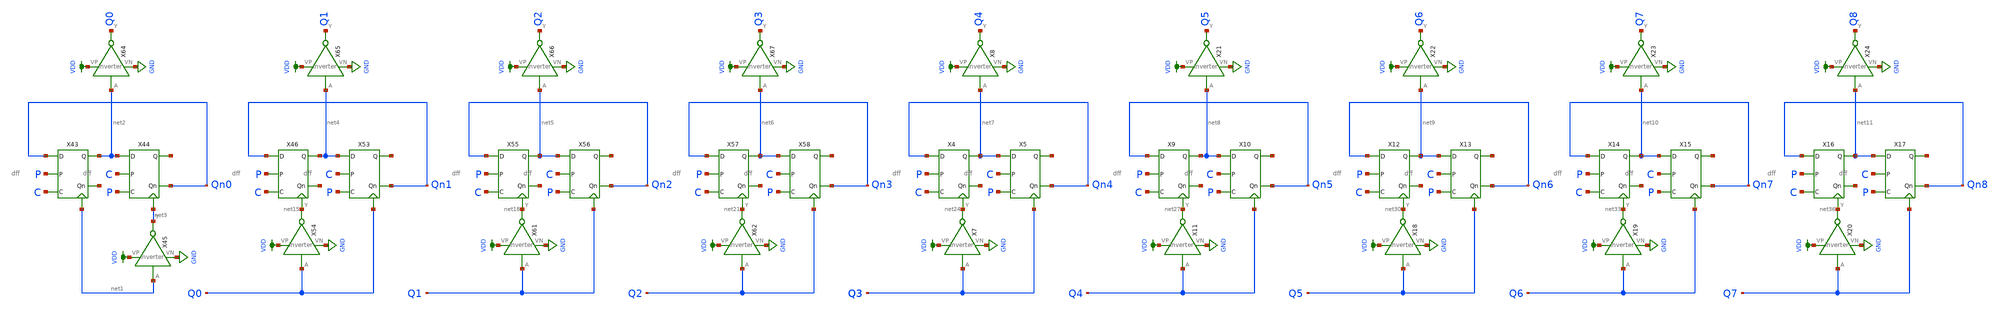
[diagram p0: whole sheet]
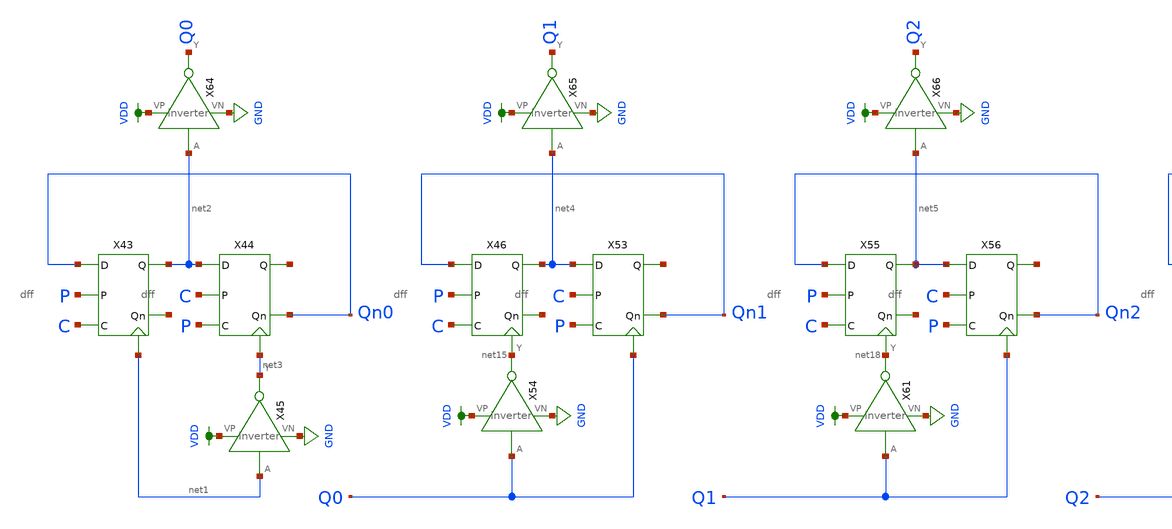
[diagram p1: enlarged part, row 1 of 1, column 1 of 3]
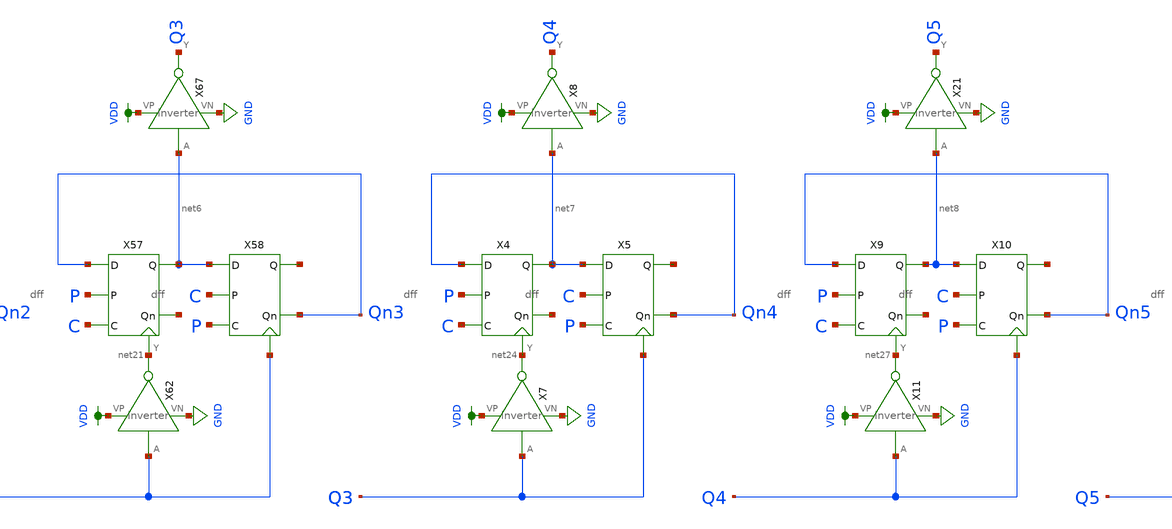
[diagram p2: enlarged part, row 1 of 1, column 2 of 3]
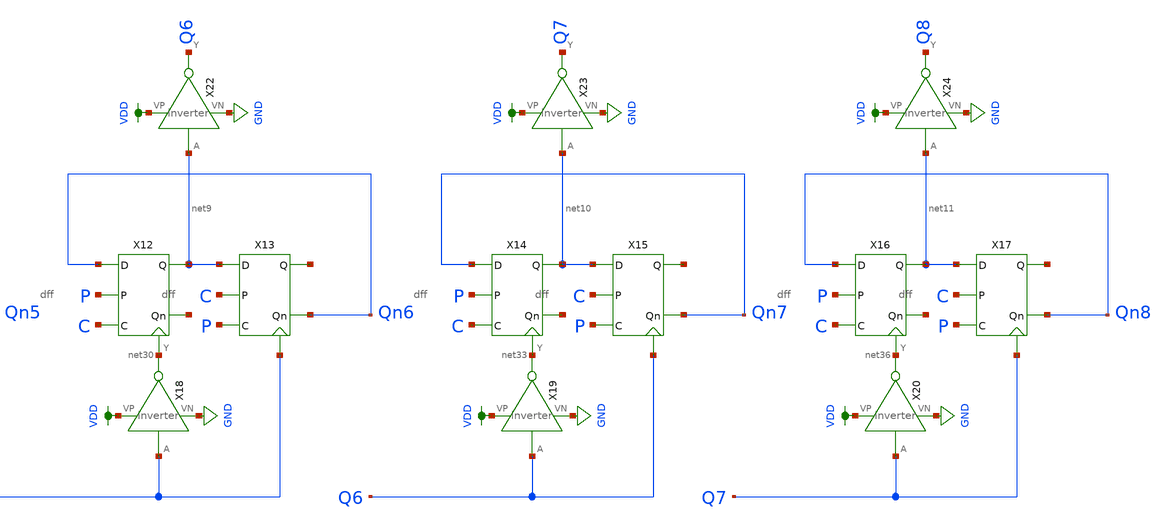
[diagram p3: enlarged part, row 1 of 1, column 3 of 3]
** sch_path: schematic/counter_lvs.sch
**.subckt counter_lvs
X43 Qn0 net12 net2 net1 P C dff
X44 net2 Qn0 net13 net3 C P dff
X45 net1 net3 VDD GND inverter
X46 Qn1 net14 net4 net15 P C dff
X53 net4 Qn1 net16 Q0 C P dff
X54 Q0 net15 VDD GND inverter
X55 Qn2 net17 net5 net18 P C dff
X56 net5 Qn2 net19 Q1 C P dff
X57 Qn3 net20 net6 net21 P C dff
X58 net6 Qn3 net22 Q2 C P dff
X61 Q1 net18 VDD GND inverter
X62 Q2 net21 VDD GND inverter
X64 net2 Q0 VDD GND inverter
X65 net4 Q1 VDD GND inverter
X66 net5 Q2 VDD GND inverter
X67 net6 Q3 VDD GND inverter
X4 Qn4 net23 net7 net24 P C dff
X5 net7 Qn4 net25 Q3 C P dff
X7 Q3 net24 VDD GND inverter
X8 net7 Q4 VDD GND inverter
X9 Qn5 net26 net8 net27 P C dff
X10 net8 Qn5 net28 Q4 C P dff
X11 Q4 net27 VDD GND inverter
X12 Qn6 net29 net9 net30 P C dff
X13 net9 Qn6 net31 Q5 C P dff
X14 Qn7 net32 net10 net33 P C dff
X15 net10 Qn7 net34 Q6 C P dff
X18 Q5 net30 VDD GND inverter
X19 Q6 net33 VDD GND inverter
X21 net8 Q5 VDD GND inverter
X22 net9 Q6 VDD GND inverter
X23 net10 Q7 VDD GND inverter
X16 Qn8 net35 net11 net36 P C dff
X17 net11 Qn8 net37 Q7 C P dff
X20 Q7 net36 VDD GND inverter
X24 net11 Q8 VDD GND inverter
**.ends
.GLOBAL VDD
.GLOBAL GND
.end
